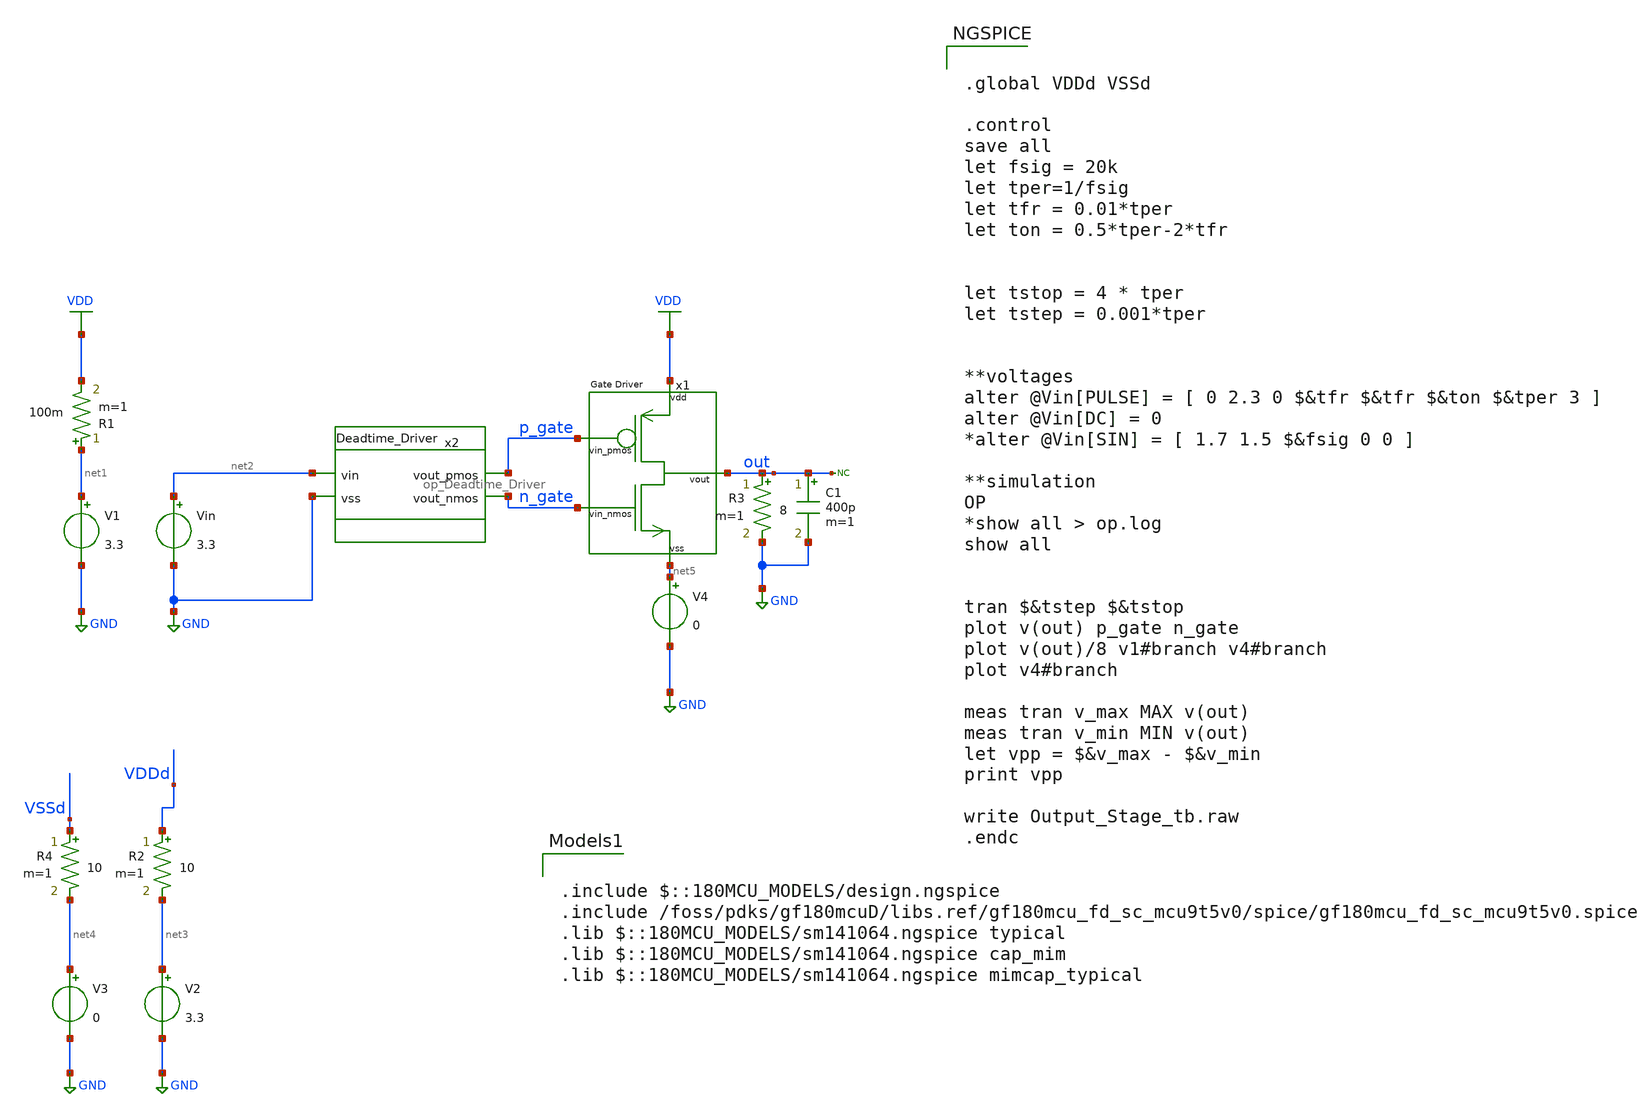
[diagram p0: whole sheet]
** sch_path: designs/libs/tb_analog_pads_pex/tb_Output_Stage/tb_Output_Stage.sch
**.subckt tb_Output_Stage
Vin net2 GND 3.3
V1 net1 GND 3.3
R1 net1 VDD 100m m=1
* noconn out
R3 out GND 8 m=1
C1 out GND 400p m=1
x1 VDD p_gate out n_gate net5 Output_Stage
x2 p_gate net2 n_gate GND op_Deadtime_Driver
V2 net3 GND 3.3
R2 VDDd net3 10 m=1
V3 net4 GND 0
R4 VSSd net4 10 m=1
V4 net5 GND 0
**** begin user architecture code


.global VDDd VSSd

.control
save all
let fsig = 20k
let tper=1/fsig
let tfr = 0.01*tper
let ton = 0.5*tper-2*tfr


let tstop = 4 * tper
let tstep = 0.001*tper


**voltages
alter @Vin[PULSE] = [ 0 2.3 0 $&tfr $&tfr $&ton $&tper 3 ]
alter @Vin[DC] = 0
*alter @Vin[SIN] = [ 1.7 1.5 $&fsig 0 0 ]

**simulation
OP
*show all > op.log
show all


tran $&tstep $&tstop
plot v(out) p_gate n_gate
plot v(out)/8 v1#branch v4#branch
plot v4#branch

meas tran v_max MAX v(out)
meas tran v_min MIN v(out)
let vpp = $&v_max - $&v_min
print vpp

write Output_Stage_tb.raw
.endc



.include $::180MCU_MODELS/design.ngspice
.include /foss/pdks/gf180mcuD/libs.ref/gf180mcu_fd_sc_mcu9t5v0/spice/gf180mcu_fd_sc_mcu9t5v0.spice
.lib $::180MCU_MODELS/sm141064.ngspice typical
.lib $::180MCU_MODELS/sm141064.ngspice cap_mim
.lib $::180MCU_MODELS/sm141064.ngspice mimcap_typical

**** end user architecture code
**.ends
.GLOBAL VDD
.GLOBAL GND
.end
